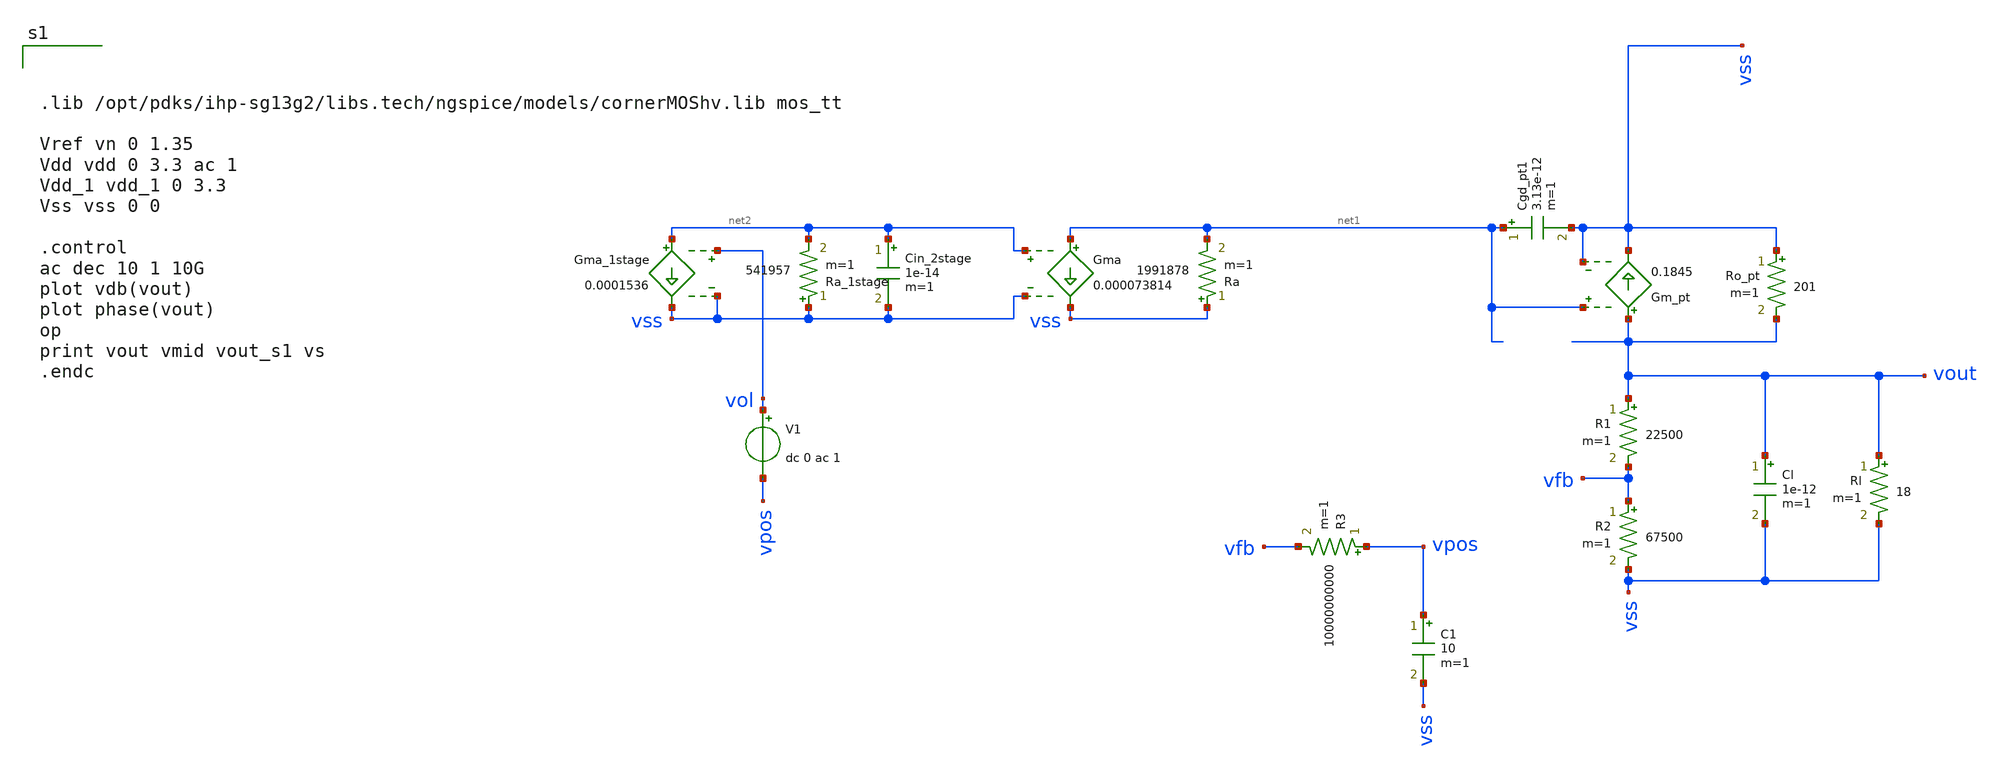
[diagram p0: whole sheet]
** sch_path: test-python/Tesis_notebooks/xschem/ldo_ol_pm_tb.sch
**.subckt ldo_ol_pm_tb
R3 vpos vfb 10000000000 m=1
C1 vpos vss 10 m=1
Ro_pt vss vout 201 m=1
Gm_pt vout vss net1 vss 0.1845
R1 vout vfb 22500 m=1
R2 vfb vss 67500 m=1
Gma net1 vss net2 vss 0.000073814
Ra vss net1 1991878 m=1
Rl vout vss 18 m=1
Cl vout vss 1e-12 m=1
Cgd_pt1 net1 vss 3.13e-12 m=1
Gma_1stage net2 vss vol vss 0.0001536
Ra_1stage vss net2 541957 m=1
V1 vol vpos dc 0 ac 1
Cin_2stage net2 vss 1e-14 m=1
**** begin user architecture code



.lib /opt/pdks/ihp-sg13g2/libs.tech/ngspice/models/cornerMOShv.lib mos_tt

Vref vn 0 1.35
Vdd vdd 0 3.3 ac 1
Vdd_1 vdd_1 0 3.3
Vss vss 0 0

.control
ac dec 10 1 10G
plot vdb(vout)
plot phase(vout)
op
print vout vmid vout_s1 vs
.endc



**** end user architecture code
**.ends
.end
